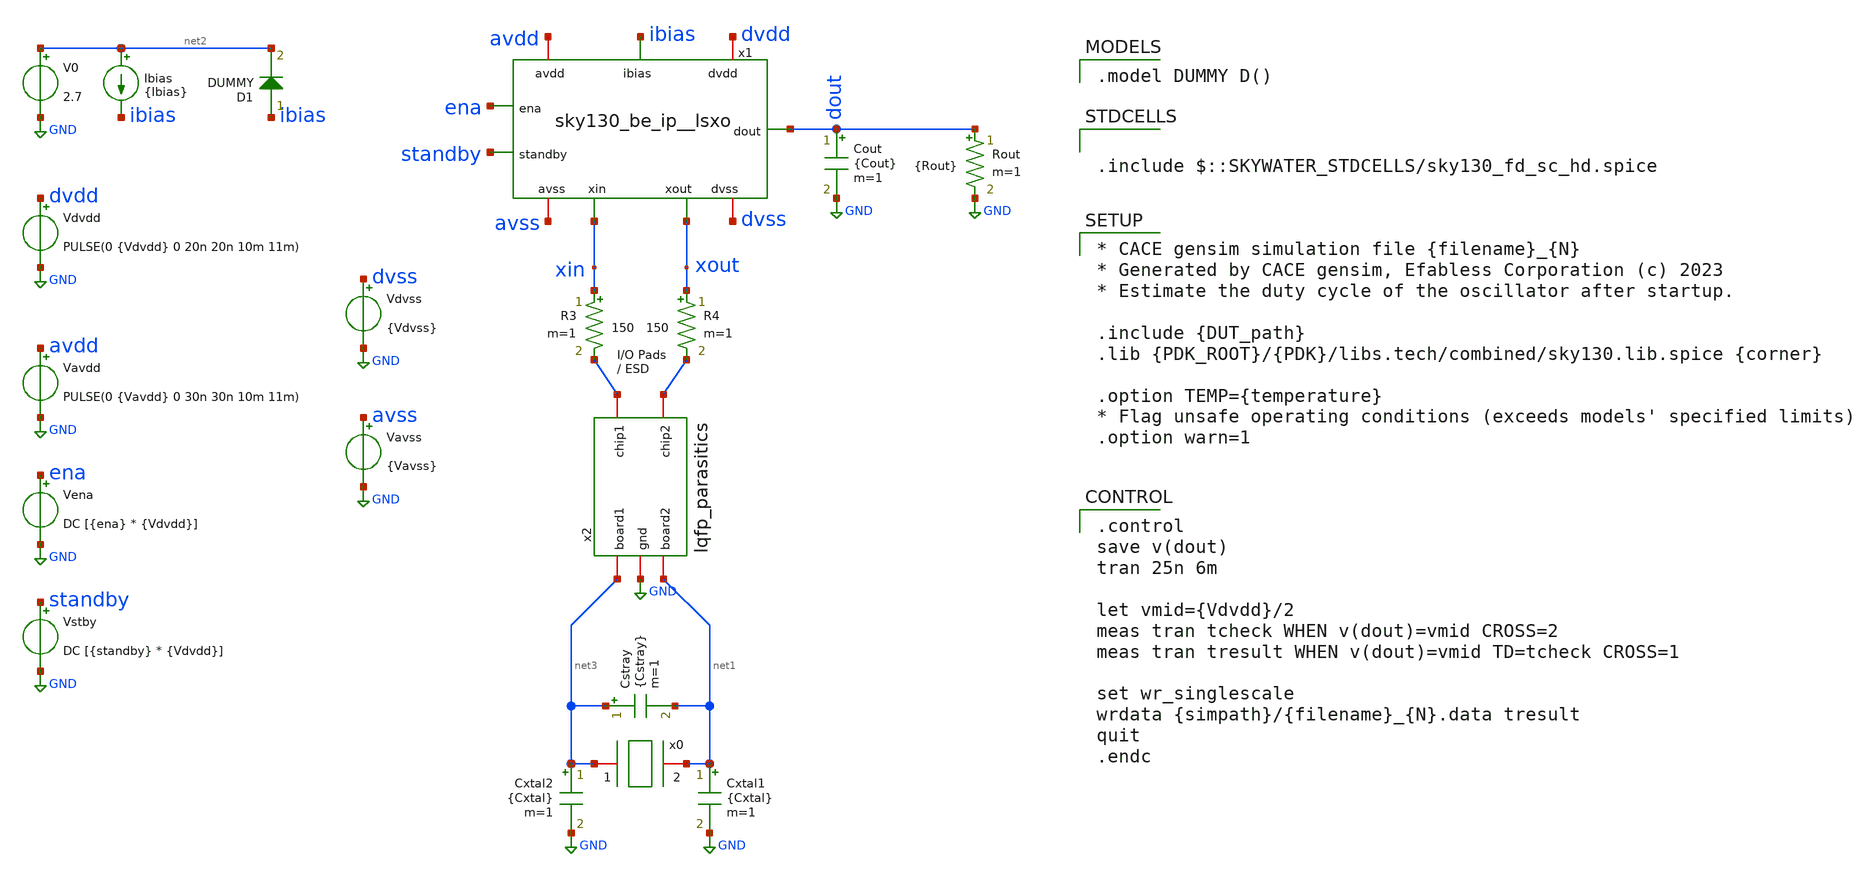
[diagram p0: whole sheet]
** sch_path: cace/tb_startup_pwron.sch

.include $::SKYWATER_STDCELLS/sky130_fd_sc_hd.spice

**.subckt tb_startup_pwron
Vdvdd dvdd GND PULSE(0 {Vdvdd} 0 20n 20n 10m 11m)
Vavdd avdd GND PULSE(0 {Vavdd} 0 30n 30n 10m 11m)
Cxtal2 net3 GND {Cxtal} m=1
Cxtal1 net1 GND {Cxtal} m=1
Cstray net3 net1 {Cstray} m=1
Ibias net2 ibias {Ibias}
Cout dout GND {Cout} m=1
V0 net2 GND 2.7
R3 xin net4 150 m=1
R4 xout net5 150 m=1
x2 net5 net4 GND net3 net1 lqfp_parasitics
D1 ibias net2 DUMMY area=100
x1 avdd avss dvdd dvss ibias ena standby dout xin xout sky130_be_ip__lsxo
Vdvss dvss GND {Vdvss}
Vavss avss GND {Vavss}
Rout dout GND {Rout} m=1
x0 net3 net1 xtal_iqd_125_1
Vena ena GND DC [{ena} * {Vdvdd}]
Vstby standby GND DC [{standby} * {Vdvdd}]
**** begin user architecture code

.model DUMMY D()


.control
save v(dout)
tran 25n 6m

let vmid={Vdvdd}/2
meas tran tcheck WHEN v(dout)=vmid CROSS=2
meas tran tresult WHEN v(dout)=vmid TD=tcheck CROSS=1

set wr_singlescale
wrdata {simpath}/{filename}_{N}.data tresult
quit
.endc



* CACE gensim simulation file {filename}_{N}
* Generated by CACE gensim, Efabless Corporation (c) 2023
* Estimate the duty cycle of the oscillator after startup.

.include {DUT_path}
.lib {PDK_ROOT}/{PDK}/libs.tech/combined/sky130.lib.spice {corner}

.option TEMP={temperature}
* Flag unsafe operating conditions (exceeds models' specified limits)
.option warn=1


**** end user architecture code
**.ends
.GLOBAL GND
.end
